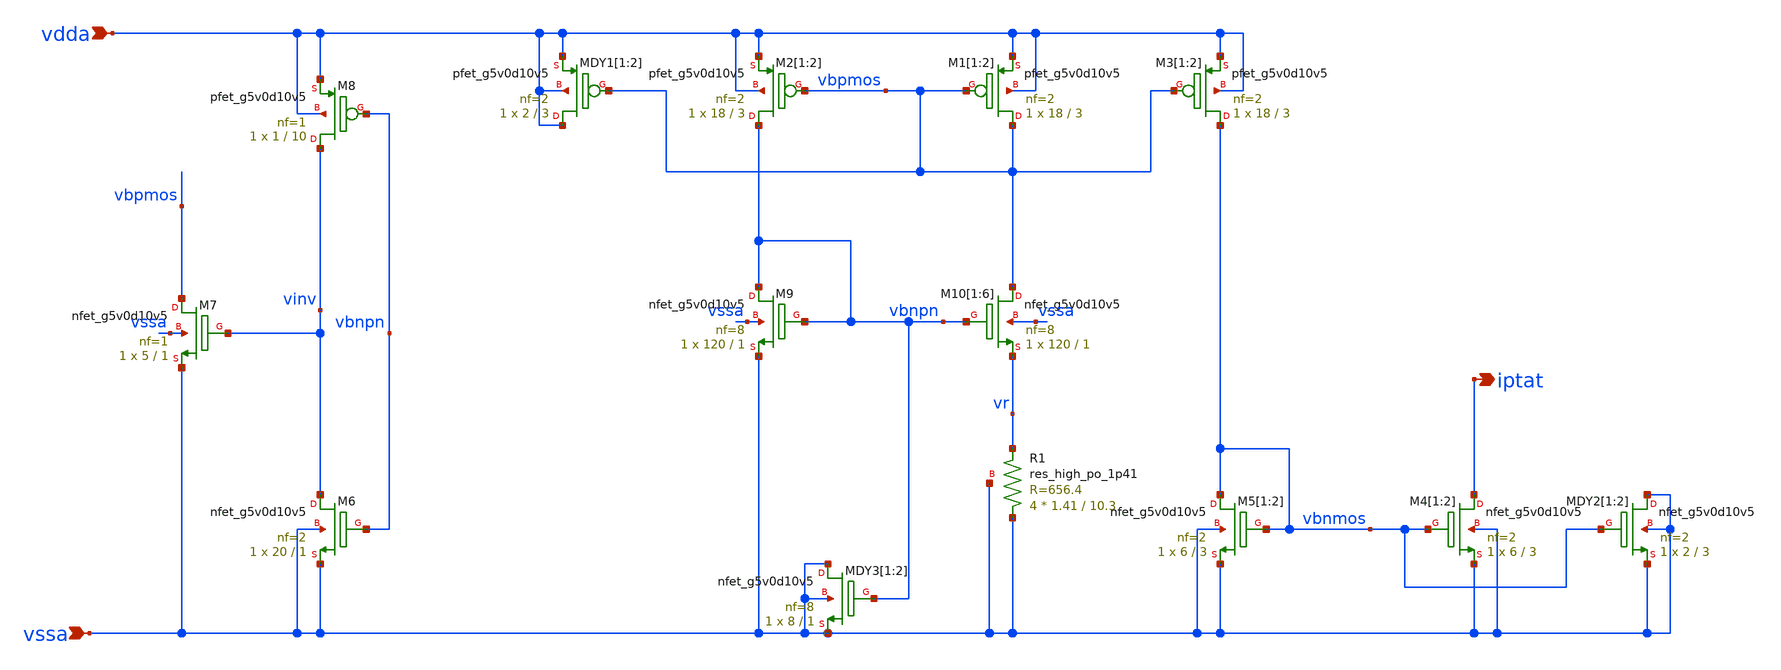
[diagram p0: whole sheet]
** sch_path: xschem/iptat.sch
**.subckt iptat vdda vssa iptat
*.ipin vdda
*.ipin vssa
*.opin iptat
XM1[1] vbpmos vbpmos vdda vdda sky130_fd_pr__pfet_g5v0d10v5 L=3 W=18 nf=2 ad='int((nf+1)/2) * W/nf * 0.29'
+ as='int((nf+2)/2) * W/nf * 0.29' pd='2*int((nf+1)/2) * (W/nf + 0.29)' ps='2*int((nf+2)/2) * (W/nf + 0.29)'
+ nrd='0.29 / W' nrs='0.29 / W' sa=0 sb=0 sd=0 mult=1 m=1
XM1[2] vbpmos vbpmos vdda vdda sky130_fd_pr__pfet_g5v0d10v5 L=3 W=18 nf=2 ad='int((nf+1)/2) * W/nf * 0.29'
+ as='int((nf+2)/2) * W/nf * 0.29' pd='2*int((nf+1)/2) * (W/nf + 0.29)' ps='2*int((nf+2)/2) * (W/nf + 0.29)'
+ nrd='0.29 / W' nrs='0.29 / W' sa=0 sb=0 sd=0 mult=1 m=1
XM2[1] vbnpn vbpmos vdda vdda sky130_fd_pr__pfet_g5v0d10v5 L=3 W=18 nf=2 ad='int((nf+1)/2) * W/nf * 0.29'
+ as='int((nf+2)/2) * W/nf * 0.29' pd='2*int((nf+1)/2) * (W/nf + 0.29)' ps='2*int((nf+2)/2) * (W/nf + 0.29)'
+ nrd='0.29 / W' nrs='0.29 / W' sa=0 sb=0 sd=0 mult=1 m=1
XM2[2] vbnpn vbpmos vdda vdda sky130_fd_pr__pfet_g5v0d10v5 L=3 W=18 nf=2 ad='int((nf+1)/2) * W/nf * 0.29'
+ as='int((nf+2)/2) * W/nf * 0.29' pd='2*int((nf+1)/2) * (W/nf + 0.29)' ps='2*int((nf+2)/2) * (W/nf + 0.29)'
+ nrd='0.29 / W' nrs='0.29 / W' sa=0 sb=0 sd=0 mult=1 m=1
XM3[1] vbnmos vbpmos vdda vdda sky130_fd_pr__pfet_g5v0d10v5 L=3 W=18 nf=2 ad='int((nf+1)/2) * W/nf * 0.29'
+ as='int((nf+2)/2) * W/nf * 0.29' pd='2*int((nf+1)/2) * (W/nf + 0.29)' ps='2*int((nf+2)/2) * (W/nf + 0.29)'
+ nrd='0.29 / W' nrs='0.29 / W' sa=0 sb=0 sd=0 mult=1 m=1
XM3[2] vbnmos vbpmos vdda vdda sky130_fd_pr__pfet_g5v0d10v5 L=3 W=18 nf=2 ad='int((nf+1)/2) * W/nf * 0.29'
+ as='int((nf+2)/2) * W/nf * 0.29' pd='2*int((nf+1)/2) * (W/nf + 0.29)' ps='2*int((nf+2)/2) * (W/nf + 0.29)'
+ nrd='0.29 / W' nrs='0.29 / W' sa=0 sb=0 sd=0 mult=1 m=1
XM4[1] iptat vbnmos vssa vssa sky130_fd_pr__nfet_g5v0d10v5 L=3 W=6 nf=2 ad='int((nf+1)/2) * W/nf * 0.29'
+ as='int((nf+2)/2) * W/nf * 0.29' pd='2*int((nf+1)/2) * (W/nf + 0.29)' ps='2*int((nf+2)/2) * (W/nf + 0.29)'
+ nrd='0.29 / W' nrs='0.29 / W' sa=0 sb=0 sd=0 mult=1 m=1
XM4[2] iptat vbnmos vssa vssa sky130_fd_pr__nfet_g5v0d10v5 L=3 W=6 nf=2 ad='int((nf+1)/2) * W/nf * 0.29'
+ as='int((nf+2)/2) * W/nf * 0.29' pd='2*int((nf+1)/2) * (W/nf + 0.29)' ps='2*int((nf+2)/2) * (W/nf + 0.29)'
+ nrd='0.29 / W' nrs='0.29 / W' sa=0 sb=0 sd=0 mult=1 m=1
XM5[1] vbnmos vbnmos vssa vssa sky130_fd_pr__nfet_g5v0d10v5 L=3 W=6 nf=2 ad='int((nf+1)/2) * W/nf * 0.29'
+ as='int((nf+2)/2) * W/nf * 0.29' pd='2*int((nf+1)/2) * (W/nf + 0.29)' ps='2*int((nf+2)/2) * (W/nf + 0.29)'
+ nrd='0.29 / W' nrs='0.29 / W' sa=0 sb=0 sd=0 mult=1 m=1
XM5[2] vbnmos vbnmos vssa vssa sky130_fd_pr__nfet_g5v0d10v5 L=3 W=6 nf=2 ad='int((nf+1)/2) * W/nf * 0.29'
+ as='int((nf+2)/2) * W/nf * 0.29' pd='2*int((nf+1)/2) * (W/nf + 0.29)' ps='2*int((nf+2)/2) * (W/nf + 0.29)'
+ nrd='0.29 / W' nrs='0.29 / W' sa=0 sb=0 sd=0 mult=1 m=1
XMDY1[1] vdda vbpmos vdda vdda sky130_fd_pr__pfet_g5v0d10v5 L=3 W=2 nf=2 ad='int((nf+1)/2) * W/nf * 0.29'
+ as='int((nf+2)/2) * W/nf * 0.29' pd='2*int((nf+1)/2) * (W/nf + 0.29)' ps='2*int((nf+2)/2) * (W/nf + 0.29)'
+ nrd='0.29 / W' nrs='0.29 / W' sa=0 sb=0 sd=0 mult=1 m=1
XMDY1[2] vdda vbpmos vdda vdda sky130_fd_pr__pfet_g5v0d10v5 L=3 W=2 nf=2 ad='int((nf+1)/2) * W/nf * 0.29'
+ as='int((nf+2)/2) * W/nf * 0.29' pd='2*int((nf+1)/2) * (W/nf + 0.29)' ps='2*int((nf+2)/2) * (W/nf + 0.29)'
+ nrd='0.29 / W' nrs='0.29 / W' sa=0 sb=0 sd=0 mult=1 m=1
XMDY2[1] vssa vbnmos vssa vssa sky130_fd_pr__nfet_g5v0d10v5 L=3 W=2 nf=2 ad='int((nf+1)/2) * W/nf * 0.29'
+ as='int((nf+2)/2) * W/nf * 0.29' pd='2*int((nf+1)/2) * (W/nf + 0.29)' ps='2*int((nf+2)/2) * (W/nf + 0.29)'
+ nrd='0.29 / W' nrs='0.29 / W' sa=0 sb=0 sd=0 mult=1 m=1
XMDY2[2] vssa vbnmos vssa vssa sky130_fd_pr__nfet_g5v0d10v5 L=3 W=2 nf=2 ad='int((nf+1)/2) * W/nf * 0.29'
+ as='int((nf+2)/2) * W/nf * 0.29' pd='2*int((nf+1)/2) * (W/nf + 0.29)' ps='2*int((nf+2)/2) * (W/nf + 0.29)'
+ nrd='0.29 / W' nrs='0.29 / W' sa=0 sb=0 sd=0 mult=1 m=1
XR1 vssa vr vssa sky130_fd_pr__res_high_po_1p41 L=10.3 mult=4 m=4
XM6 vinv vbnpn vssa vssa sky130_fd_pr__nfet_g5v0d10v5 L=1 W=20 nf=2 ad='int((nf+1)/2) * W/nf * 0.29'
+ as='int((nf+2)/2) * W/nf * 0.29' pd='2*int((nf+1)/2) * (W/nf + 0.29)' ps='2*int((nf+2)/2) * (W/nf + 0.29)'
+ nrd='0.29 / W' nrs='0.29 / W' sa=0 sb=0 sd=0 mult=1 m=1
XM7 vbpmos vinv vssa vssa sky130_fd_pr__nfet_g5v0d10v5 L=1 W=5 nf=1 ad='int((nf+1)/2) * W/nf * 0.29'
+ as='int((nf+2)/2) * W/nf * 0.29' pd='2*int((nf+1)/2) * (W/nf + 0.29)' ps='2*int((nf+2)/2) * (W/nf + 0.29)'
+ nrd='0.29 / W' nrs='0.29 / W' sa=0 sb=0 sd=0 mult=1 m=1
XM8 vinv vbnpn vdda vdda sky130_fd_pr__pfet_g5v0d10v5 L=10 W=1 nf=1 ad='int((nf+1)/2) * W/nf * 0.29'
+ as='int((nf+2)/2) * W/nf * 0.29' pd='2*int((nf+1)/2) * (W/nf + 0.29)' ps='2*int((nf+2)/2) * (W/nf + 0.29)'
+ nrd='0.29 / W' nrs='0.29 / W' sa=0 sb=0 sd=0 mult=1 m=1
XM9 vbnpn vbnpn vssa vssa sky130_fd_pr__nfet_g5v0d10v5 L=1 W=120 nf=8 ad='int((nf+1)/2) * W/nf * 0.29'
+ as='int((nf+2)/2) * W/nf * 0.29' pd='2*int((nf+1)/2) * (W/nf + 0.29)' ps='2*int((nf+2)/2) * (W/nf + 0.29)'
+ nrd='0.29 / W' nrs='0.29 / W' sa=0 sb=0 sd=0 mult=1 m=1
XM10[1] vbpmos vbnpn vr vssa sky130_fd_pr__nfet_g5v0d10v5 L=1 W=120 nf=8 ad='int((nf+1)/2) * W/nf * 0.29'
+ as='int((nf+2)/2) * W/nf * 0.29' pd='2*int((nf+1)/2) * (W/nf + 0.29)' ps='2*int((nf+2)/2) * (W/nf + 0.29)'
+ nrd='0.29 / W' nrs='0.29 / W' sa=0 sb=0 sd=0 mult=1 m=1
XM10[2] vbpmos vbnpn vr vssa sky130_fd_pr__nfet_g5v0d10v5 L=1 W=120 nf=8 ad='int((nf+1)/2) * W/nf * 0.29'
+ as='int((nf+2)/2) * W/nf * 0.29' pd='2*int((nf+1)/2) * (W/nf + 0.29)' ps='2*int((nf+2)/2) * (W/nf + 0.29)'
+ nrd='0.29 / W' nrs='0.29 / W' sa=0 sb=0 sd=0 mult=1 m=1
XM10[3] vbpmos vbnpn vr vssa sky130_fd_pr__nfet_g5v0d10v5 L=1 W=120 nf=8 ad='int((nf+1)/2) * W/nf * 0.29'
+ as='int((nf+2)/2) * W/nf * 0.29' pd='2*int((nf+1)/2) * (W/nf + 0.29)' ps='2*int((nf+2)/2) * (W/nf + 0.29)'
+ nrd='0.29 / W' nrs='0.29 / W' sa=0 sb=0 sd=0 mult=1 m=1
XM10[4] vbpmos vbnpn vr vssa sky130_fd_pr__nfet_g5v0d10v5 L=1 W=120 nf=8 ad='int((nf+1)/2) * W/nf * 0.29'
+ as='int((nf+2)/2) * W/nf * 0.29' pd='2*int((nf+1)/2) * (W/nf + 0.29)' ps='2*int((nf+2)/2) * (W/nf + 0.29)'
+ nrd='0.29 / W' nrs='0.29 / W' sa=0 sb=0 sd=0 mult=1 m=1
XM10[5] vbpmos vbnpn vr vssa sky130_fd_pr__nfet_g5v0d10v5 L=1 W=120 nf=8 ad='int((nf+1)/2) * W/nf * 0.29'
+ as='int((nf+2)/2) * W/nf * 0.29' pd='2*int((nf+1)/2) * (W/nf + 0.29)' ps='2*int((nf+2)/2) * (W/nf + 0.29)'
+ nrd='0.29 / W' nrs='0.29 / W' sa=0 sb=0 sd=0 mult=1 m=1
XM10[6] vbpmos vbnpn vr vssa sky130_fd_pr__nfet_g5v0d10v5 L=1 W=120 nf=8 ad='int((nf+1)/2) * W/nf * 0.29'
+ as='int((nf+2)/2) * W/nf * 0.29' pd='2*int((nf+1)/2) * (W/nf + 0.29)' ps='2*int((nf+2)/2) * (W/nf + 0.29)'
+ nrd='0.29 / W' nrs='0.29 / W' sa=0 sb=0 sd=0 mult=1 m=1
XMDY3[1] vssa vbnpn vssa vssa sky130_fd_pr__nfet_g5v0d10v5 L=1 W=8 nf=8 ad='int((nf+1)/2) * W/nf * 0.29'
+ as='int((nf+2)/2) * W/nf * 0.29' pd='2*int((nf+1)/2) * (W/nf + 0.29)' ps='2*int((nf+2)/2) * (W/nf + 0.29)'
+ nrd='0.29 / W' nrs='0.29 / W' sa=0 sb=0 sd=0 mult=1 m=1
XMDY3[2] vssa vbnpn vssa vssa sky130_fd_pr__nfet_g5v0d10v5 L=1 W=8 nf=8 ad='int((nf+1)/2) * W/nf * 0.29'
+ as='int((nf+2)/2) * W/nf * 0.29' pd='2*int((nf+1)/2) * (W/nf + 0.29)' ps='2*int((nf+2)/2) * (W/nf + 0.29)'
+ nrd='0.29 / W' nrs='0.29 / W' sa=0 sb=0 sd=0 mult=1 m=1
**.ends
.end
